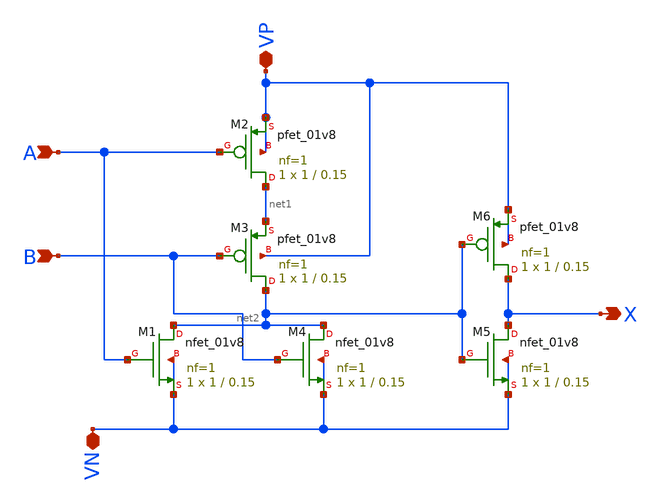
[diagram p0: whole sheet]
** sch_path: projekat_spice/layout/or/OR.sch
**.subckt OR X A B VP VN
*.opin X
*.ipin A
*.ipin B
*.iopin VP
*.iopin VN
XM1 net2 A VN VN sky130_fd_pr__nfet_01v8 L=0.15 W=1 nf=1 ad='int((nf+1)/2) * W/nf * 0.29' as='int((nf+2)/2) * W/nf * 0.29'
+ pd='2*int((nf+1)/2) * (W/nf + 0.29)' ps='2*int((nf+2)/2) * (W/nf + 0.29)' nrd='0.29 / W' nrs='0.29 / W'
+ sa=0 sb=0 sd=0 mult=1 m=1
XM2 net1 A VP VP sky130_fd_pr__pfet_01v8 L=0.15 W=1 nf=1 ad='int((nf+1)/2) * W/nf * 0.29' as='int((nf+2)/2) * W/nf * 0.29'
+ pd='2*int((nf+1)/2) * (W/nf + 0.29)' ps='2*int((nf+2)/2) * (W/nf + 0.29)' nrd='0.29 / W' nrs='0.29 / W'
+ sa=0 sb=0 sd=0 mult=1 m=1
XM3 net2 B net1 VP sky130_fd_pr__pfet_01v8 L=0.15 W=1 nf=1 ad='int((nf+1)/2) * W/nf * 0.29' as='int((nf+2)/2) * W/nf * 0.29'
+ pd='2*int((nf+1)/2) * (W/nf + 0.29)' ps='2*int((nf+2)/2) * (W/nf + 0.29)' nrd='0.29 / W' nrs='0.29 / W'
+ sa=0 sb=0 sd=0 mult=1 m=1
XM4 net2 B VN VN sky130_fd_pr__nfet_01v8 L=0.15 W=1 nf=1 ad='int((nf+1)/2) * W/nf * 0.29' as='int((nf+2)/2) * W/nf * 0.29'
+ pd='2*int((nf+1)/2) * (W/nf + 0.29)' ps='2*int((nf+2)/2) * (W/nf + 0.29)' nrd='0.29 / W' nrs='0.29 / W'
+ sa=0 sb=0 sd=0 mult=1 m=1
XM5 X net2 VN VN sky130_fd_pr__nfet_01v8 L=0.15 W=1 nf=1 ad='int((nf+1)/2) * W/nf * 0.29' as='int((nf+2)/2) * W/nf * 0.29'
+ pd='2*int((nf+1)/2) * (W/nf + 0.29)' ps='2*int((nf+2)/2) * (W/nf + 0.29)' nrd='0.29 / W' nrs='0.29 / W'
+ sa=0 sb=0 sd=0 mult=1 m=1
XM6 X net2 VP VP sky130_fd_pr__pfet_01v8 L=0.15 W=1 nf=1 ad='int((nf+1)/2) * W/nf * 0.29' as='int((nf+2)/2) * W/nf * 0.29'
+ pd='2*int((nf+1)/2) * (W/nf + 0.29)' ps='2*int((nf+2)/2) * (W/nf + 0.29)' nrd='0.29 / W' nrs='0.29 / W'
+ sa=0 sb=0 sd=0 mult=1 m=1
**.ends
.end
